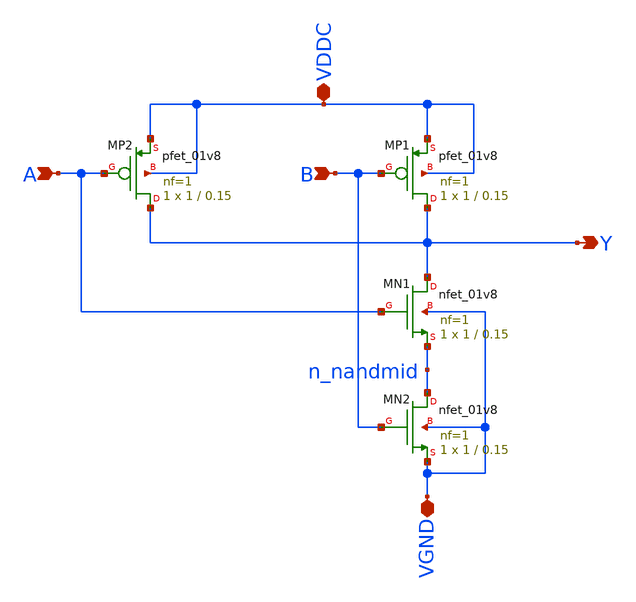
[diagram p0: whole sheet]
** sch_path: designs/bgr_ldo/ldo/ro_nand.sch
**.subckt ro_nand VDDC VGND A Y B
*.iopin VDDC
*.iopin VGND
*.ipin A
*.opin Y
*.ipin B
XMP1 Y B VDDC VDDC sky130_fd_pr__pfet_01v8 L=0.15 W=1 nf=1 ad='int((1 + 1)/2) * 1 / 1 * 0.29' as='int((1 + 2)/2) * 1 / 1 * 0.29'
+ pd='2*int((1 + 1)/2) * (1 / 1 + 0.29)' ps='2*int((1 + 2)/2) * (1 / 1 + 0.29)' nrd='0.29 / 1 ' nrs='0.29 / 1 '
+ sa=0 sb=0 sd=0 mult=1 m=1
XMP2 Y A VDDC VDDC sky130_fd_pr__pfet_01v8 L=0.15 W=1 nf=1 ad='int((1 + 1)/2) * 1 / 1 * 0.29' as='int((1 + 2)/2) * 1 / 1 * 0.29'
+ pd='2*int((1 + 1)/2) * (1 / 1 + 0.29)' ps='2*int((1 + 2)/2) * (1 / 1 + 0.29)' nrd='0.29 / 1 ' nrs='0.29 / 1 '
+ sa=0 sb=0 sd=0 mult=1 m=1
XMN1 Y A n_nandmid VGND sky130_fd_pr__nfet_01v8 L=0.15 W=1 nf=1 ad='int((1 + 1)/2) * 1 / 1 * 0.29' as='int((1 + 2)/2) * 1 / 1 * 0.29'
+ pd='2*int((1 + 1)/2) * (1 / 1 + 0.29)' ps='2*int((1 + 2)/2) * (1 / 1 + 0.29)' nrd='0.29 / 1 ' nrs='0.29 / 1 '
+ sa=0 sb=0 sd=0 mult=1 m=1
XMN2 n_nandmid B VGND VGND sky130_fd_pr__nfet_01v8 L=0.15 W=1 nf=1 ad='int((1 + 1)/2) * 1 / 1 * 0.29'
+ as='int((1 + 2)/2) * 1 / 1 * 0.29' pd='2*int((1 + 1)/2) * (1 / 1 + 0.29)' ps='2*int((1 + 2)/2) * (1 / 1 + 0.29)'
+ nrd='0.29 / 1 ' nrs='0.29 / 1 ' sa=0 sb=0 sd=0 mult=1 m=1
**.ends
.end
